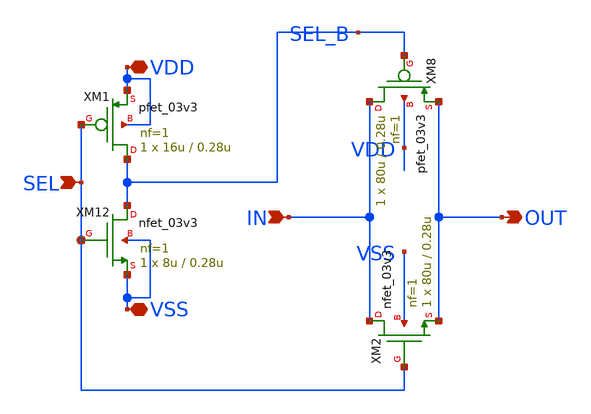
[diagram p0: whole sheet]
** sch_path: DAC_PAKISTAN_01/Pakistan1_Xschem/TG.sch
**.subckt TG VDD VSS IN SEL OUT
*.iopin VDD
*.iopin VSS
*.ipin IN
*.ipin SEL
*.opin OUT
XM8 IN SEL_B OUT VDD pfet_03v3 L=0.28u W=80u nf=1 ad='int((nf+1)/2) * W/nf * 0.18u' as='int((nf+2)/2) * W/nf * 0.18u'
+ pd='2*int((nf+1)/2) * (W/nf + 0.18u)' ps='2*int((nf+2)/2) * (W/nf + 0.18u)' nrd='0.18u / W' nrs='0.18u / W'
+ sa=0 sb=0 sd=0 m=1
XM12 SEL_B SEL VSS VSS nfet_03v3 L=0.28u W=8u nf=1 ad='int((nf+1)/2) * W/nf * 0.18u' as='int((nf+2)/2) * W/nf * 0.18u'
+ pd='2*int((nf+1)/2) * (W/nf + 0.18u)' ps='2*int((nf+2)/2) * (W/nf + 0.18u)' nrd='0.18u / W' nrs='0.18u / W'
+ sa=0 sb=0 sd=0 m=1
XM1 SEL_B SEL VDD VDD pfet_03v3 L=0.28u W=16u nf=1 ad='int((nf+1)/2) * W/nf * 0.18u' as='int((nf+2)/2) * W/nf * 0.18u'
+ pd='2*int((nf+1)/2) * (W/nf + 0.18u)' ps='2*int((nf+2)/2) * (W/nf + 0.18u)' nrd='0.18u / W' nrs='0.18u / W'
+ sa=0 sb=0 sd=0 m=1
XM2 IN SEL OUT VSS nfet_03v3 L=0.28u W=80u nf=1 ad='int((nf+1)/2) * W/nf * 0.18u' as='int((nf+2)/2) * W/nf * 0.18u'
+ pd='2*int((nf+1)/2) * (W/nf + 0.18u)' ps='2*int((nf+2)/2) * (W/nf + 0.18u)' nrd='0.18u / W' nrs='0.18u / W'
+ sa=0 sb=0 sd=0 m=1
**.ends
.end
